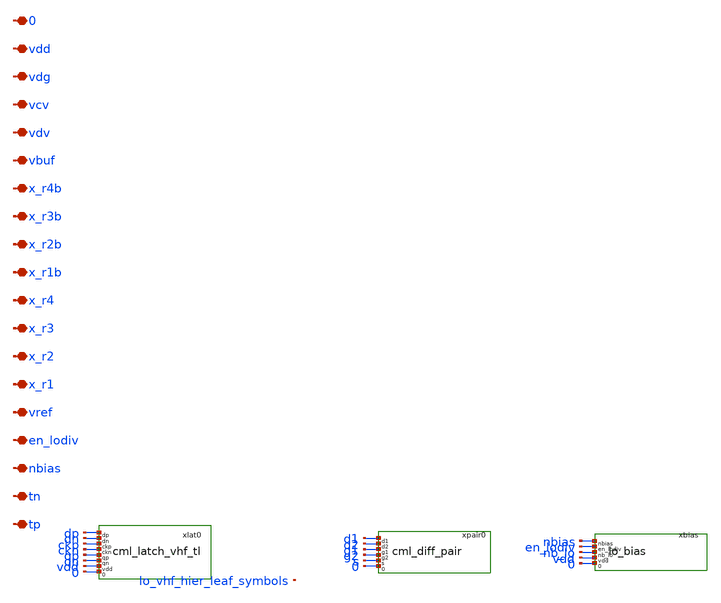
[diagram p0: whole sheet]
** sch_path: analog/lo/sch/lo_vhf_hier.sch
**.subckt lo_vhf_hier tp tn nbias en_lodiv vref x_r1 x_r2 x_r3 x_r4 x_r1b x_r2b x_r3b x_r4b vbuf vdv
*+ vcv vdg vdd 0
*.iopin tp
*.iopin tn
*.iopin nbias
*.iopin en_lodiv
*.iopin vref
*.iopin x_r1
*.iopin x_r2
*.iopin x_r3
*.iopin x_r4
*.iopin x_r1b
*.iopin x_r2b
*.iopin x_r3b
*.iopin x_r4b
*.iopin vbuf
*.iopin vdv
*.iopin vcv
*.iopin vdg
*.iopin vdd
*.iopin 0
xlat0 dp dn ckp ckn qp qn vdd 0 cml_latch_vhf_tl
xpair0 d1 d2 g1 g2 s 0 cml_diff_pair
xbias nbias en_lodiv nb_lo vdd 0 lo_bias
**.ends

* expanding   symbol:  cml_latch_vhf_tl.sym # of pins=8
** sym_path: analog/lo/sch/cml_latch_vhf_tl.sym
** sch_path: analog/lo/sch/cml_latch_vhf_tl.sch
.subckt cml_latch_vhf_tl dp dn ckp ckn qp qn vdd 0
*.iopin dp
*.iopin dn
*.iopin ckp
*.iopin ckn
*.iopin qp
*.iopin qn
*.iopin vdd
*.iopin 0
rlap vdd qp 666.7 m=1
rlan vdd qn 666.7 m=1
Xma1 qn dp s1a 0 sg13_lv_nmos w=7.50u l=0.13u ng=1 m=1 mm_ok=1
Xma2 qp dn s1a 0 sg13_lv_nmos w=7.50u l=0.13u ng=1 m=1 mm_ok=1
Xma3 qn qp s2a 0 sg13_lv_nmos w=11.25u l=0.13u ng=1 m=1 mm_ok=1
Xma4 qp qn s2a 0 sg13_lv_nmos w=11.25u l=0.13u ng=1 m=1 mm_ok=1
Xma5 s1a ckp 0 0 sg13_lv_nmos w=7.50u l=0.13u ng=1 m=1 mm_ok=1
Xma6 s2a ckn 0 0 sg13_lv_nmos w=7.50u l=0.13u ng=1 m=1 mm_ok=1
.ends


* expanding   symbol:  cml_diff_pair.sym # of pins=6
** sym_path: analog/lo/sch/cml_diff_pair.sym
** sch_path: analog/lo/sch/cml_diff_pair.sch
.subckt cml_diff_pair d1 d2 g1 g2 s 0
*.iopin d1
*.iopin d2
*.iopin g1
*.iopin g2
*.iopin s
*.iopin 0
Xmm1 d1 g1 s 0 sg13_lv_nmos w=7.50u l=0.13u ng=1 m=1 mm_ok=1
Xmm2 d2 g2 s 0 sg13_lv_nmos w=7.50u l=0.13u ng=1 m=1 mm_ok=1
.ends


* expanding   symbol:  lo_bias.sym # of pins=5
** sym_path: analog/lo/sch/lo_bias.sym
** sch_path: analog/lo/sch/lo_bias.sch
.subckt lo_bias nbias en_lodiv nb_lo vdd 0
*.iopin nbias
*.iopin en_lodiv
*.iopin nb_lo
*.iopin vdd
*.iopin 0
Xxenb_p en_n en_lodiv vdd vdd sg13_lv_pmos w=1u l=0.13u ng=1 m=1 mm_ok=1
Xxenb_n en_n en_lodiv 0 0 sg13_lv_nmos w=0.5u l=0.13u ng=1 m=1 mm_ok=1
Xtgn nb_lo en_lodiv nbias 0 sg13_lv_nmos w=4u l=0.13u ng=1 m=1 mm_ok=1
Xtgp nb_lo en_n nbias vdd sg13_lv_pmos w=8u l=0.13u ng=1 m=1 mm_ok=1
Xmpd nb_lo en_n 0 0 sg13_lv_nmos w=2u l=0.13u ng=1 m=1 mm_ok=1
.ends

.end
